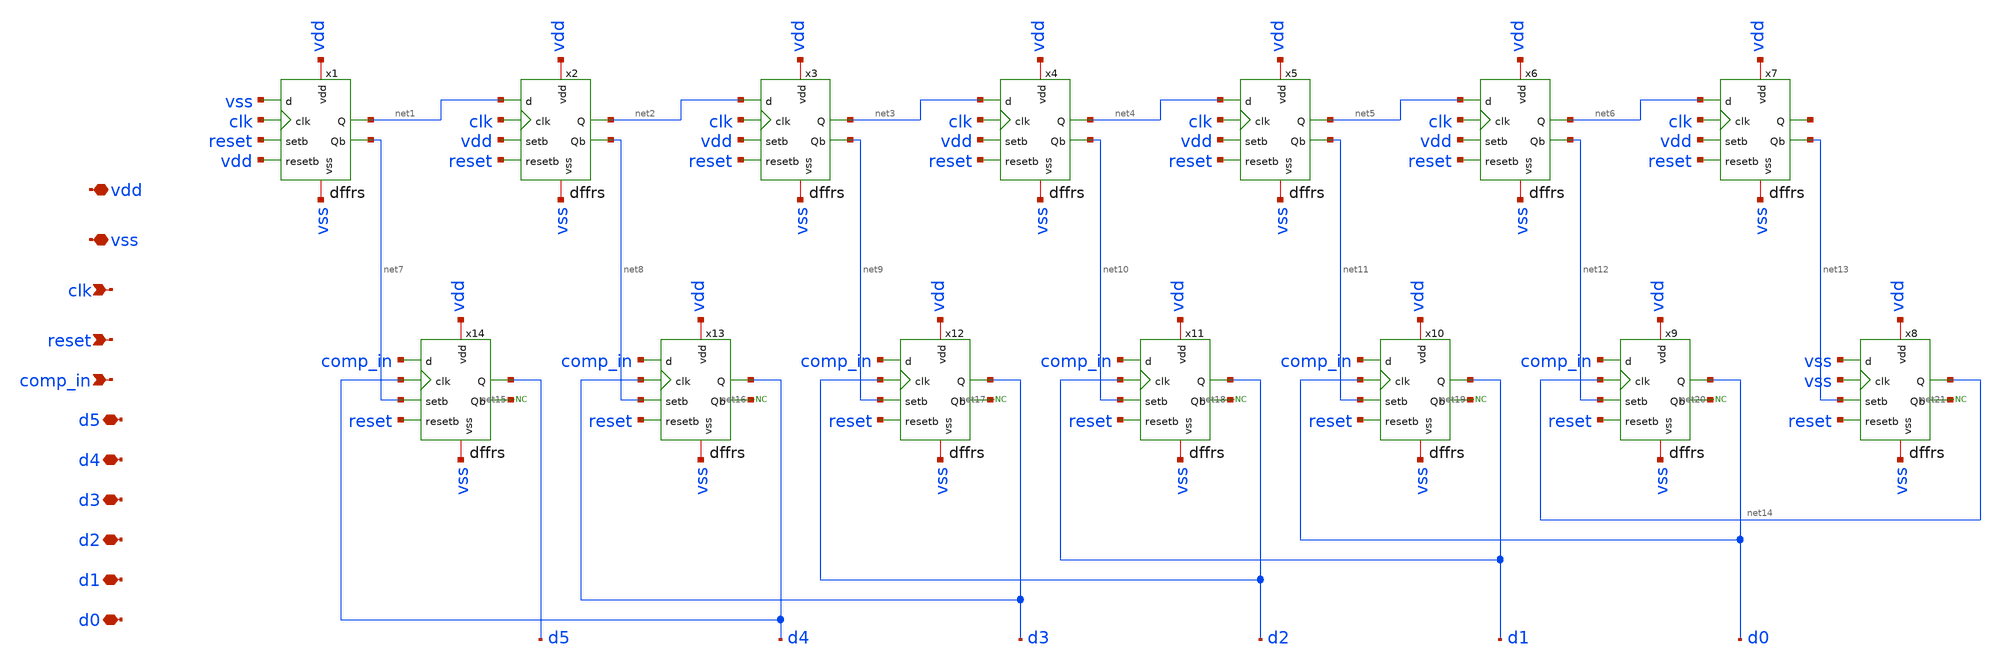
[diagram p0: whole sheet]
** sch_path: designs/FinalBlocksLayout/SARlogic/SARlogic.sch
**.subckt SARlogic comp_in vdd vss clk reset d5 d4 d3 d2 d1 d0
*.ipin comp_in
*.iopin vdd
*.iopin vss
*.ipin clk
*.ipin reset
*.iopin d5
*.iopin d4
*.iopin d3
*.iopin d2
*.iopin d1
*.iopin d0
* noconn #net15
* noconn #net16
* noconn #net17
* noconn #net18
* noconn #net19
* noconn #net20
* noconn #net21
x1 vdd vss vss clk reset vdd net1 net7 dffrs
x2 vdd vss net1 clk vdd reset net2 net8 dffrs
x3 vdd vss net2 clk vdd reset net3 net9 dffrs
x4 vdd vss net3 clk vdd reset net4 net10 dffrs
x5 vdd vss net4 clk vdd reset net5 net11 dffrs
x6 vdd vss net5 clk vdd reset net6 net12 dffrs
x7 vdd vss net6 clk vdd reset net22 net13 dffrs
x8 vdd vss vss vss net13 reset net14 net21 dffrs
x9 vdd vss comp_in net14 net12 reset d0 net20 dffrs
x10 vdd vss comp_in d0 net11 reset d1 net19 dffrs
x11 vdd vss comp_in d1 net10 reset d2 net18 dffrs
x12 vdd vss comp_in d2 net9 reset d3 net17 dffrs
x13 vdd vss comp_in d3 net8 reset d4 net16 dffrs
x14 vdd vss comp_in d4 net7 reset d5 net15 dffrs
**.ends
.end
